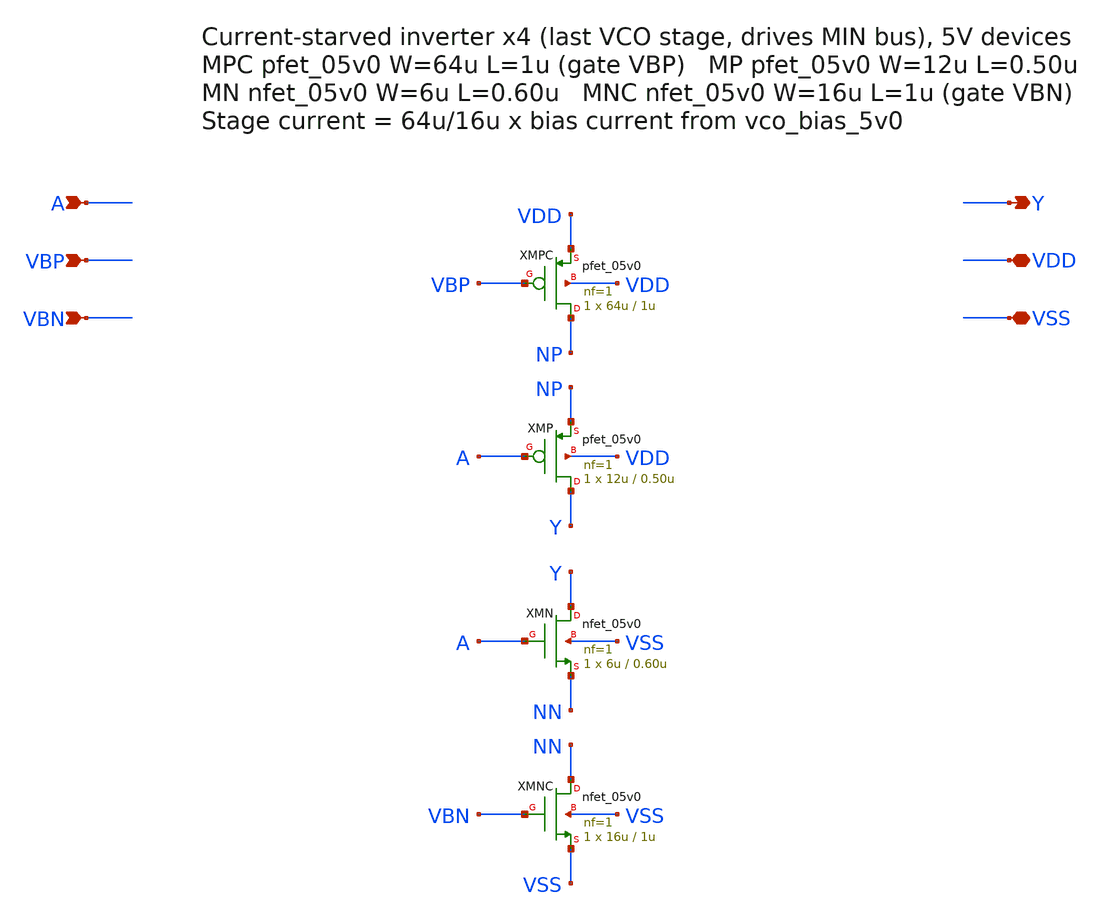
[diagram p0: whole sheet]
** sch_path: vco/cs_inv_x4_5v0.sch
**.subckt cs_inv_x4_5v0 A Y VBP VDD VBN VSS
*.ipin A
*.opin Y
*.ipin VBP
*.iopin VDD
*.ipin VBN
*.iopin VSS
XMPC NP VBP VDD VDD pfet_05v0 L=1u W=64u nf=1 ad='int((nf+1)/2) * W/nf * 0.18u' as='int((nf+2)/2) * W/nf * 0.18u'
+ pd='2*int((nf+1)/2) * (W/nf + 0.18u)' ps='2*int((nf+2)/2) * (W/nf + 0.18u)' nrd='0.18u / W' nrs='0.18u / W'
+ sa=0 sb=0 sd=0 m=1
XMP Y A NP VDD pfet_05v0 L=0.50u W=12u nf=1 ad='int((nf+1)/2) * W/nf * 0.18u' as='int((nf+2)/2) * W/nf * 0.18u'
+ pd='2*int((nf+1)/2) * (W/nf + 0.18u)' ps='2*int((nf+2)/2) * (W/nf + 0.18u)' nrd='0.18u / W' nrs='0.18u / W'
+ sa=0 sb=0 sd=0 m=1
XMN Y A NN VSS nfet_05v0 L=0.60u W=6u nf=1 ad='int((nf+1)/2) * W/nf * 0.18u' as='int((nf+2)/2) * W/nf * 0.18u'
+ pd='2*int((nf+1)/2) * (W/nf + 0.18u)' ps='2*int((nf+2)/2) * (W/nf + 0.18u)' nrd='0.18u / W' nrs='0.18u / W'
+ sa=0 sb=0 sd=0 m=1
XMNC NN VBN VSS VSS nfet_05v0 L=1u W=16u nf=1 ad='int((nf+1)/2) * W/nf * 0.18u' as='int((nf+2)/2) * W/nf * 0.18u'
+ pd='2*int((nf+1)/2) * (W/nf + 0.18u)' ps='2*int((nf+2)/2) * (W/nf + 0.18u)' nrd='0.18u / W' nrs='0.18u / W'
+ sa=0 sb=0 sd=0 m=1
**.ends
.end
